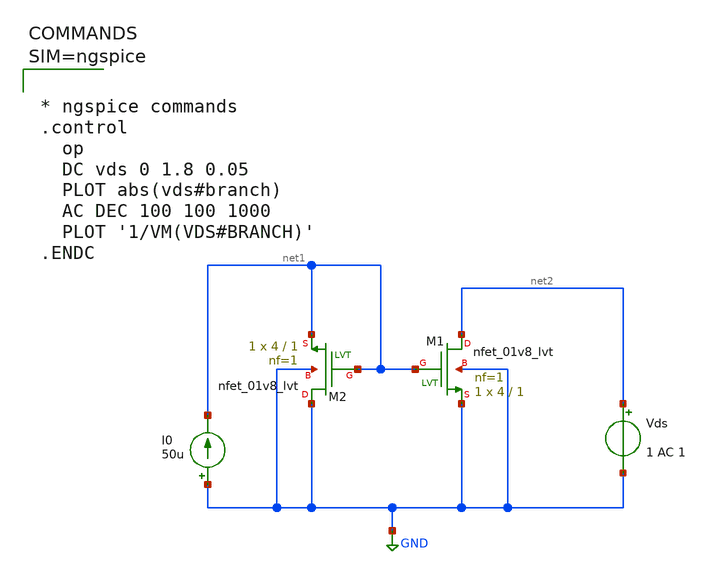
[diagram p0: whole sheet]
** sch_path: xschem/untitled-10.sch
**.subckt untitled-10
XM1 net2 net1 GND GND sky130_fd_pr__nfet_01v8_lvt L=1 W=4 nf=1 ad='int((1 + 1)/2) * 4 / 1 * 0.29' as='int((1 + 2)/2) * 4 / 1 * 0.29'
+ pd='2*int((1 + 1)/2) * (4 / 1 + 0.29)' ps='2*int((1 + 2)/2) * (4 / 1 + 0.29)' nrd='0.29 / 4 ' nrs='0.29 / 4 '
+ sa=0 sb=0 sd=0 mult=1 m=1
XM2 GND net1 net1 GND sky130_fd_pr__nfet_01v8_lvt L=1 W=4 nf=1 ad='int((1 + 1)/2) * 4 / 1 * 0.29' as='int((1 + 2)/2) * 4 / 1 * 0.29'
+ pd='2*int((1 + 1)/2) * (4 / 1 + 0.29)' ps='2*int((1 + 2)/2) * (4 / 1 + 0.29)' nrd='0.29 / 4 ' nrs='0.29 / 4 '
+ sa=0 sb=0 sd=0 mult=1 m=1
Vds net2 GND 1 AC 1
I0 GND net1 50u
**** begin user architecture code



* ngspice commands
.control
  op
  DC vds 0 1.8 0.05
  PLOT abs(vds#branch)
  AC DEC 100 100 1000
  PLOT '1/VM(VDS#BRANCH)'
.ENDC




** opencircuitdesign pdks install
.lib $::SKYWATER_MODELS/sky130.lib.spice tt

**** end user architecture code
**.ends
.GLOBAL GND
.end
